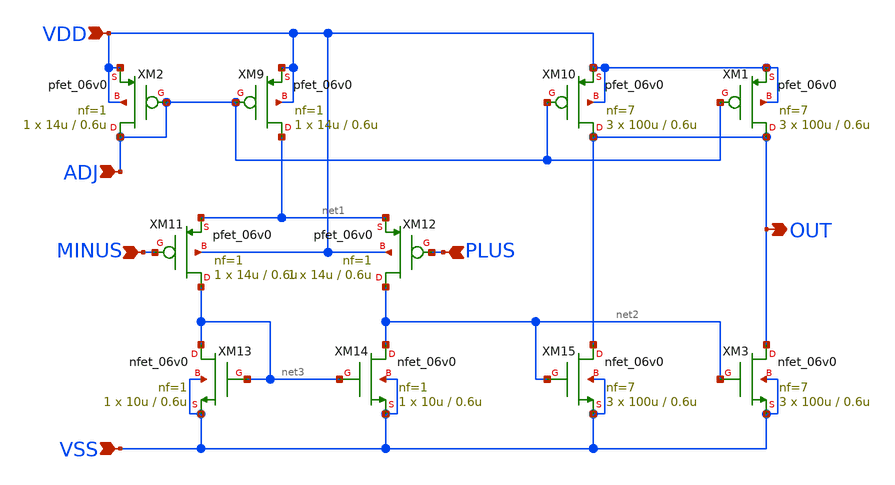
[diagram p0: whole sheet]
** sch_path: macros/Analog/R2R_DAC/xschem/opamp_chonky.sch
**.subckt opamp_chonky VDD PLUS VSS OUT MINUS ADJ
*.ipin VDD
*.ipin PLUS
*.ipin VSS
*.opin OUT
*.ipin MINUS
*.ipin ADJ
XM2 ADJ ADJ VDD VDD pfet_06v0 L=0.6u W=14u nf=1 ad='int((nf+1)/2) * W/nf * 0.18u' as='int((nf+2)/2) * W/nf * 0.18u'
+ pd='2*int((nf+1)/2) * (W/nf + 0.18u)' ps='2*int((nf+2)/2) * (W/nf + 0.18u)' nrd='0.18u / W' nrs='0.18u / W'
+ sa=0 sb=0 sd=0 m=1
XM9 net1 ADJ VDD VDD pfet_06v0 L=0.6u W=14u nf=1 ad='int((nf+1)/2) * W/nf * 0.18u' as='int((nf+2)/2) * W/nf * 0.18u'
+ pd='2*int((nf+1)/2) * (W/nf + 0.18u)' ps='2*int((nf+2)/2) * (W/nf + 0.18u)' nrd='0.18u / W' nrs='0.18u / W'
+ sa=0 sb=0 sd=0 m=1
XM10 OUT ADJ VDD VDD pfet_06v0 L=0.6u W=100u nf=7 ad='int((nf+1)/2) * W/nf * 0.18u' as='int((nf+2)/2) * W/nf * 0.18u'
+ pd='2*int((nf+1)/2) * (W/nf + 0.18u)' ps='2*int((nf+2)/2) * (W/nf + 0.18u)' nrd='0.18u / W' nrs='0.18u / W'
+ sa=0 sb=0 sd=0 m=3
XM11 net3 MINUS net1 VDD pfet_06v0 L=0.6u W=14u nf=1 ad='int((nf+1)/2) * W/nf * 0.18u' as='int((nf+2)/2) * W/nf * 0.18u'
+ pd='2*int((nf+1)/2) * (W/nf + 0.18u)' ps='2*int((nf+2)/2) * (W/nf + 0.18u)' nrd='0.18u / W' nrs='0.18u / W'
+ sa=0 sb=0 sd=0 m=1
XM12 net2 PLUS net1 VDD pfet_06v0 L=0.6u W=14u nf=1 ad='int((nf+1)/2) * W/nf * 0.18u' as='int((nf+2)/2) * W/nf * 0.18u'
+ pd='2*int((nf+1)/2) * (W/nf + 0.18u)' ps='2*int((nf+2)/2) * (W/nf + 0.18u)' nrd='0.18u / W' nrs='0.18u / W'
+ sa=0 sb=0 sd=0 m=1
XM13 net3 net3 VSS VSS nfet_06v0 L=0.6u W=10u nf=1 ad='int((nf+1)/2) * W/nf * 0.18u' as='int((nf+2)/2) * W/nf * 0.18u'
+ pd='2*int((nf+1)/2) * (W/nf + 0.18u)' ps='2*int((nf+2)/2) * (W/nf + 0.18u)' nrd='0.18u / W' nrs='0.18u / W'
+ sa=0 sb=0 sd=0 m=1
XM14 net2 net3 VSS VSS nfet_06v0 L=0.6u W=10u nf=1 ad='int((nf+1)/2) * W/nf * 0.18u' as='int((nf+2)/2) * W/nf * 0.18u'
+ pd='2*int((nf+1)/2) * (W/nf + 0.18u)' ps='2*int((nf+2)/2) * (W/nf + 0.18u)' nrd='0.18u / W' nrs='0.18u / W'
+ sa=0 sb=0 sd=0 m=1
XM15 OUT net2 VSS VSS nfet_06v0 L=0.6u W=100u nf=7 ad='int((nf+1)/2) * W/nf * 0.18u' as='int((nf+2)/2) * W/nf * 0.18u'
+ pd='2*int((nf+1)/2) * (W/nf + 0.18u)' ps='2*int((nf+2)/2) * (W/nf + 0.18u)' nrd='0.18u / W' nrs='0.18u / W'
+ sa=0 sb=0 sd=0 m=3
XM1 OUT ADJ VDD VDD pfet_06v0 L=0.6u W=100u nf=7 ad='int((nf+1)/2) * W/nf * 0.18u' as='int((nf+2)/2) * W/nf * 0.18u'
+ pd='2*int((nf+1)/2) * (W/nf + 0.18u)' ps='2*int((nf+2)/2) * (W/nf + 0.18u)' nrd='0.18u / W' nrs='0.18u / W'
+ sa=0 sb=0 sd=0 m=3
XM3 OUT net2 VSS VSS nfet_06v0 L=0.6u W=100u nf=7 ad='int((nf+1)/2) * W/nf * 0.18u' as='int((nf+2)/2) * W/nf * 0.18u'
+ pd='2*int((nf+1)/2) * (W/nf + 0.18u)' ps='2*int((nf+2)/2) * (W/nf + 0.18u)' nrd='0.18u / W' nrs='0.18u / W'
+ sa=0 sb=0 sd=0 m=3
**.ends
.end
